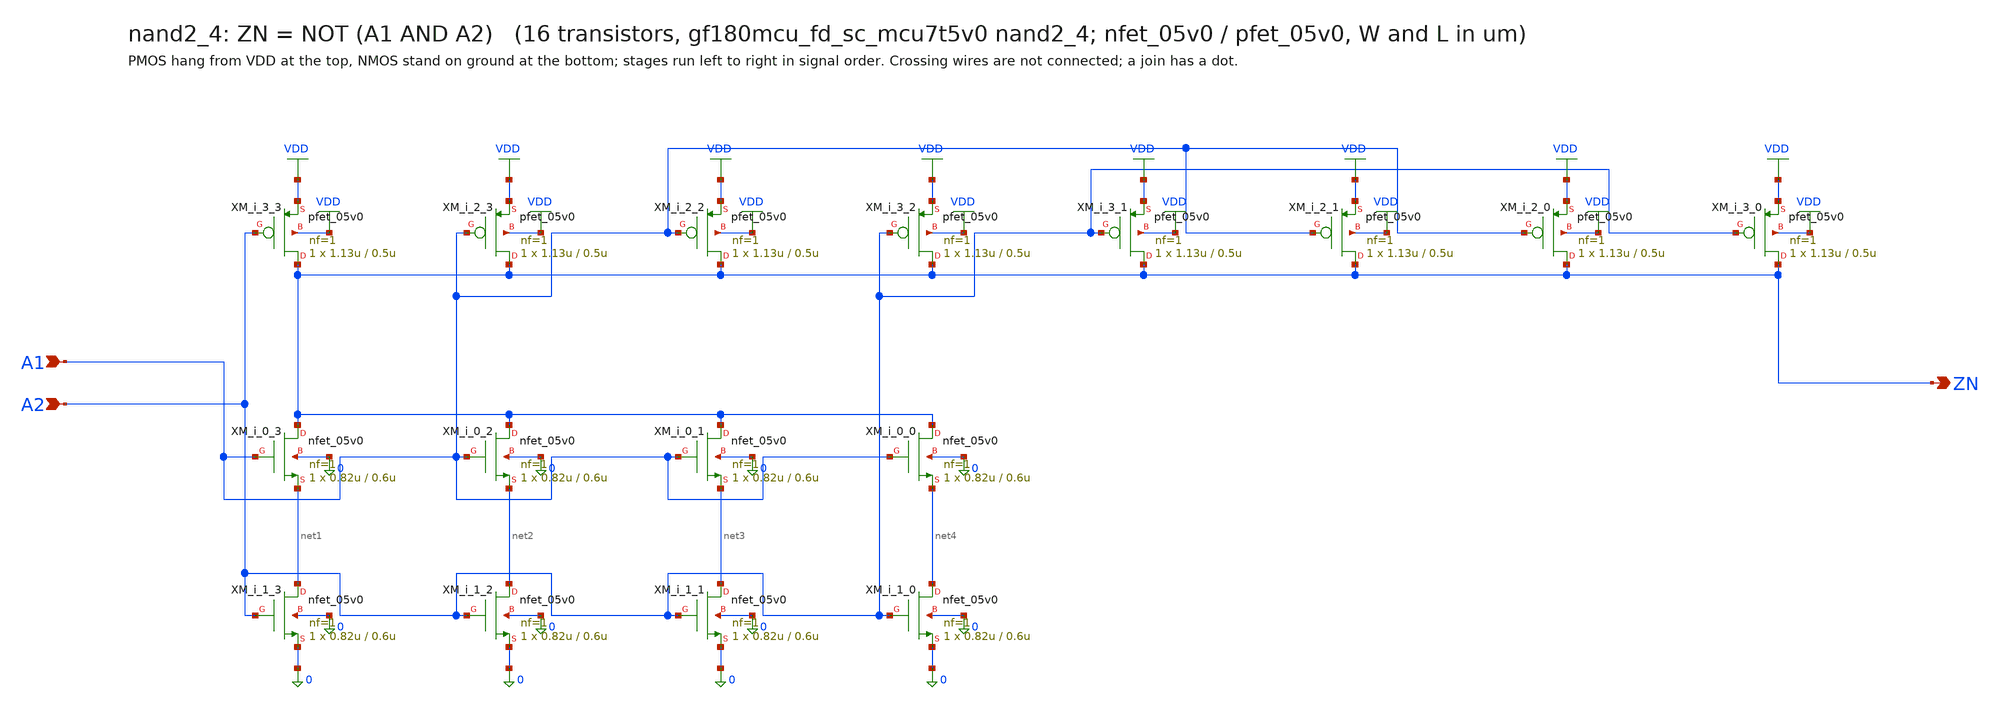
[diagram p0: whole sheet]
** sch_path: xschem/cells_tx/nand2_4.sch
**.subckt nand2_4 A1 A2 ZN
*.ipin A1
*.ipin A2
*.opin ZN
XM_i_1_3 net1 A2 0 0 nfet_05v0 L=0.6u W=0.82u nf=1 ad=4.1e-13 as=4.1e-13 pd=2.64e-06 ps=2.64e-06
+ nrd=0 nrs=0 sa=0 sb=0 sd=0 m=1
XM_i_0_3 ZN A1 net1 0 nfet_05v0 L=0.6u W=0.82u nf=1 ad=4.1e-13 as=4.1e-13 pd=2.64e-06 ps=2.64e-06
+ nrd=0 nrs=0 sa=0 sb=0 sd=0 m=1
XM_i_0_2 ZN A1 net2 0 nfet_05v0 L=0.6u W=0.82u nf=1 ad=4.1e-13 as=4.1e-13 pd=2.64e-06 ps=2.64e-06
+ nrd=0 nrs=0 sa=0 sb=0 sd=0 m=1
XM_i_1_2 net2 A2 0 0 nfet_05v0 L=0.6u W=0.82u nf=1 ad=4.1e-13 as=4.1e-13 pd=2.64e-06 ps=2.64e-06
+ nrd=0 nrs=0 sa=0 sb=0 sd=0 m=1
XM_i_1_1 net3 A2 0 0 nfet_05v0 L=0.6u W=0.82u nf=1 ad=4.1e-13 as=4.1e-13 pd=2.64e-06 ps=2.64e-06
+ nrd=0 nrs=0 sa=0 sb=0 sd=0 m=1
XM_i_0_1 ZN A1 net3 0 nfet_05v0 L=0.6u W=0.82u nf=1 ad=4.1e-13 as=4.1e-13 pd=2.64e-06 ps=2.64e-06
+ nrd=0 nrs=0 sa=0 sb=0 sd=0 m=1
XM_i_0_0 ZN A1 net4 0 nfet_05v0 L=0.6u W=0.82u nf=1 ad=4.1e-13 as=4.1e-13 pd=2.64e-06 ps=2.64e-06
+ nrd=0 nrs=0 sa=0 sb=0 sd=0 m=1
XM_i_1_0 net4 A2 0 0 nfet_05v0 L=0.6u W=0.82u nf=1 ad=4.1e-13 as=4.1e-13 pd=2.64e-06 ps=2.64e-06
+ nrd=0 nrs=0 sa=0 sb=0 sd=0 m=1
XM_i_3_3 ZN A2 VDD VDD pfet_05v0 L=0.5u W=1.13u nf=1 ad=5.65e-13 as=5.65e-13 pd=3.26e-06 ps=3.26e-06
+ nrd=0 nrs=0 sa=0 sb=0 sd=0 m=1
XM_i_2_3 ZN A1 VDD VDD pfet_05v0 L=0.5u W=1.13u nf=1 ad=5.65e-13 as=5.65e-13 pd=3.26e-06 ps=3.26e-06
+ nrd=0 nrs=0 sa=0 sb=0 sd=0 m=1
XM_i_2_2 ZN A1 VDD VDD pfet_05v0 L=0.5u W=1.13u nf=1 ad=5.65e-13 as=5.65e-13 pd=3.26e-06 ps=3.26e-06
+ nrd=0 nrs=0 sa=0 sb=0 sd=0 m=1
XM_i_3_2 ZN A2 VDD VDD pfet_05v0 L=0.5u W=1.13u nf=1 ad=5.65e-13 as=5.65e-13 pd=3.26e-06 ps=3.26e-06
+ nrd=0 nrs=0 sa=0 sb=0 sd=0 m=1
XM_i_3_1 ZN A2 VDD VDD pfet_05v0 L=0.5u W=1.13u nf=1 ad=5.65e-13 as=5.65e-13 pd=3.26e-06 ps=3.26e-06
+ nrd=0 nrs=0 sa=0 sb=0 sd=0 m=1
XM_i_2_1 ZN A1 VDD VDD pfet_05v0 L=0.5u W=1.13u nf=1 ad=5.65e-13 as=5.65e-13 pd=3.26e-06 ps=3.26e-06
+ nrd=0 nrs=0 sa=0 sb=0 sd=0 m=1
XM_i_2_0 ZN A1 VDD VDD pfet_05v0 L=0.5u W=1.13u nf=1 ad=5.65e-13 as=5.65e-13 pd=3.26e-06 ps=3.26e-06
+ nrd=0 nrs=0 sa=0 sb=0 sd=0 m=1
XM_i_3_0 ZN A2 VDD VDD pfet_05v0 L=0.5u W=1.13u nf=1 ad=5.65e-13 as=5.65e-13 pd=3.26e-06 ps=3.26e-06
+ nrd=0 nrs=0 sa=0 sb=0 sd=0 m=1
**.ends
.GLOBAL VDD
.end
